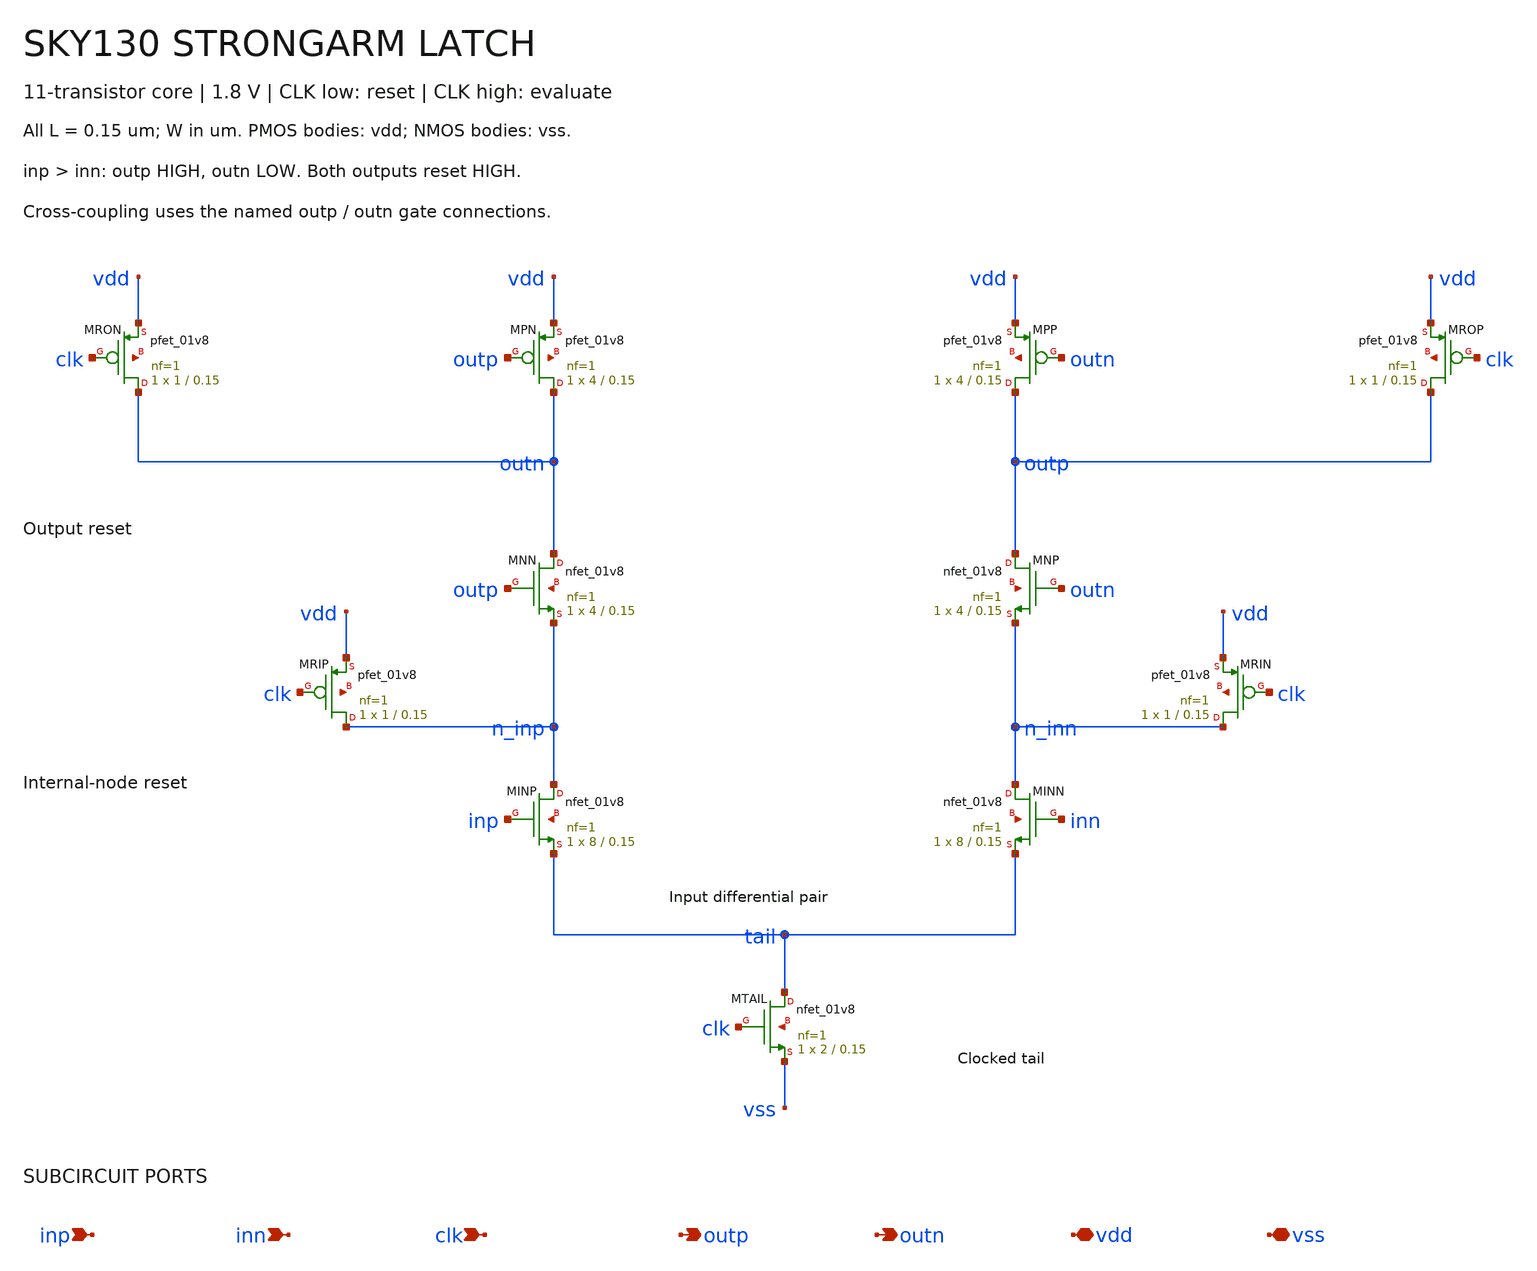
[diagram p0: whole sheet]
** sch_path: schematics/strongarm.sch
**.subckt strongarm inp inn clk outp outn vdd vss
*.ipin inp
*.ipin inn
*.ipin clk
*.opin outp
*.opin outn
*.iopin vdd
*.iopin vss
XMPN outn outp vdd vdd sky130_fd_pr__pfet_01v8 L=0.15 W=4 nf=1 ad='int((1 + 1)/2) * 4 / 1 * 0.29' as='int((1 + 2)/2) * 4 / 1 * 0.29'
+ pd='2*int((1 + 1)/2) * (4 / 1 + 0.29)' ps='2*int((1 + 2)/2) * (4 / 1 + 0.29)' nrd='0.29 / 4 ' nrs='0.29 / 4 '
+ sa=0 sb=0 sd=0 mult=1 m=1
XMPP outp outn vdd vdd sky130_fd_pr__pfet_01v8 L=0.15 W=4 nf=1 ad='int((1 + 1)/2) * 4 / 1 * 0.29' as='int((1 + 2)/2) * 4 / 1 * 0.29'
+ pd='2*int((1 + 1)/2) * (4 / 1 + 0.29)' ps='2*int((1 + 2)/2) * (4 / 1 + 0.29)' nrd='0.29 / 4 ' nrs='0.29 / 4 '
+ sa=0 sb=0 sd=0 mult=1 m=1
XMNN outn outp n_inp vss sky130_fd_pr__nfet_01v8 L=0.15 W=4 nf=1 ad='int((1 + 1)/2) * 4 / 1 * 0.29' as='int((1 + 2)/2) * 4 / 1 * 0.29'
+ pd='2*int((1 + 1)/2) * (4 / 1 + 0.29)' ps='2*int((1 + 2)/2) * (4 / 1 + 0.29)' nrd='0.29 / 4 ' nrs='0.29 / 4 '
+ sa=0 sb=0 sd=0 mult=1 m=1
XMNP outp outn n_inn vss sky130_fd_pr__nfet_01v8 L=0.15 W=4 nf=1 ad='int((1 + 1)/2) * 4 / 1 * 0.29' as='int((1 + 2)/2) * 4 / 1 * 0.29'
+ pd='2*int((1 + 1)/2) * (4 / 1 + 0.29)' ps='2*int((1 + 2)/2) * (4 / 1 + 0.29)' nrd='0.29 / 4 ' nrs='0.29 / 4 '
+ sa=0 sb=0 sd=0 mult=1 m=1
XMINP n_inp inp tail vss sky130_fd_pr__nfet_01v8 L=0.15 W=8 nf=1 ad='int((1 + 1)/2) * 8 / 1 * 0.29' as='int((1 + 2)/2) * 8 / 1 * 0.29'
+ pd='2*int((1 + 1)/2) * (8 / 1 + 0.29)' ps='2*int((1 + 2)/2) * (8 / 1 + 0.29)' nrd='0.29 / 8 ' nrs='0.29 / 8 '
+ sa=0 sb=0 sd=0 mult=1 m=1
XMINN n_inn inn tail vss sky130_fd_pr__nfet_01v8 L=0.15 W=8 nf=1 ad='int((1 + 1)/2) * 8 / 1 * 0.29' as='int((1 + 2)/2) * 8 / 1 * 0.29'
+ pd='2*int((1 + 1)/2) * (8 / 1 + 0.29)' ps='2*int((1 + 2)/2) * (8 / 1 + 0.29)' nrd='0.29 / 8 ' nrs='0.29 / 8 '
+ sa=0 sb=0 sd=0 mult=1 m=1
XMTAIL tail clk vss vss sky130_fd_pr__nfet_01v8 L=0.15 W=2 nf=1 ad='int((1 + 1)/2) * 2 / 1 * 0.29' as='int((1 + 2)/2) * 2 / 1 * 0.29'
+ pd='2*int((1 + 1)/2) * (2 / 1 + 0.29)' ps='2*int((1 + 2)/2) * (2 / 1 + 0.29)' nrd='0.29 / 2 ' nrs='0.29 / 2 '
+ sa=0 sb=0 sd=0 mult=1 m=1
XMRON outn clk vdd vdd sky130_fd_pr__pfet_01v8 L=0.15 W=1 nf=1 ad='int((1 + 1)/2) * 1 / 1 * 0.29' as='int((1 + 2)/2) * 1 / 1 * 0.29'
+ pd='2*int((1 + 1)/2) * (1 / 1 + 0.29)' ps='2*int((1 + 2)/2) * (1 / 1 + 0.29)' nrd='0.29 / 1 ' nrs='0.29 / 1 '
+ sa=0 sb=0 sd=0 mult=1 m=1
XMROP outp clk vdd vdd sky130_fd_pr__pfet_01v8 L=0.15 W=1 nf=1 ad='int((1 + 1)/2) * 1 / 1 * 0.29' as='int((1 + 2)/2) * 1 / 1 * 0.29'
+ pd='2*int((1 + 1)/2) * (1 / 1 + 0.29)' ps='2*int((1 + 2)/2) * (1 / 1 + 0.29)' nrd='0.29 / 1 ' nrs='0.29 / 1 '
+ sa=0 sb=0 sd=0 mult=1 m=1
XMRIP n_inp clk vdd vdd sky130_fd_pr__pfet_01v8 L=0.15 W=1 nf=1 ad='int((1 + 1)/2) * 1 / 1 * 0.29' as='int((1 + 2)/2) * 1 / 1 * 0.29'
+ pd='2*int((1 + 1)/2) * (1 / 1 + 0.29)' ps='2*int((1 + 2)/2) * (1 / 1 + 0.29)' nrd='0.29 / 1 ' nrs='0.29 / 1 '
+ sa=0 sb=0 sd=0 mult=1 m=1
XMRIN n_inn clk vdd vdd sky130_fd_pr__pfet_01v8 L=0.15 W=1 nf=1 ad='int((1 + 1)/2) * 1 / 1 * 0.29' as='int((1 + 2)/2) * 1 / 1 * 0.29'
+ pd='2*int((1 + 1)/2) * (1 / 1 + 0.29)' ps='2*int((1 + 2)/2) * (1 / 1 + 0.29)' nrd='0.29 / 1 ' nrs='0.29 / 1 '
+ sa=0 sb=0 sd=0 mult=1 m=1
**.ends
.end
